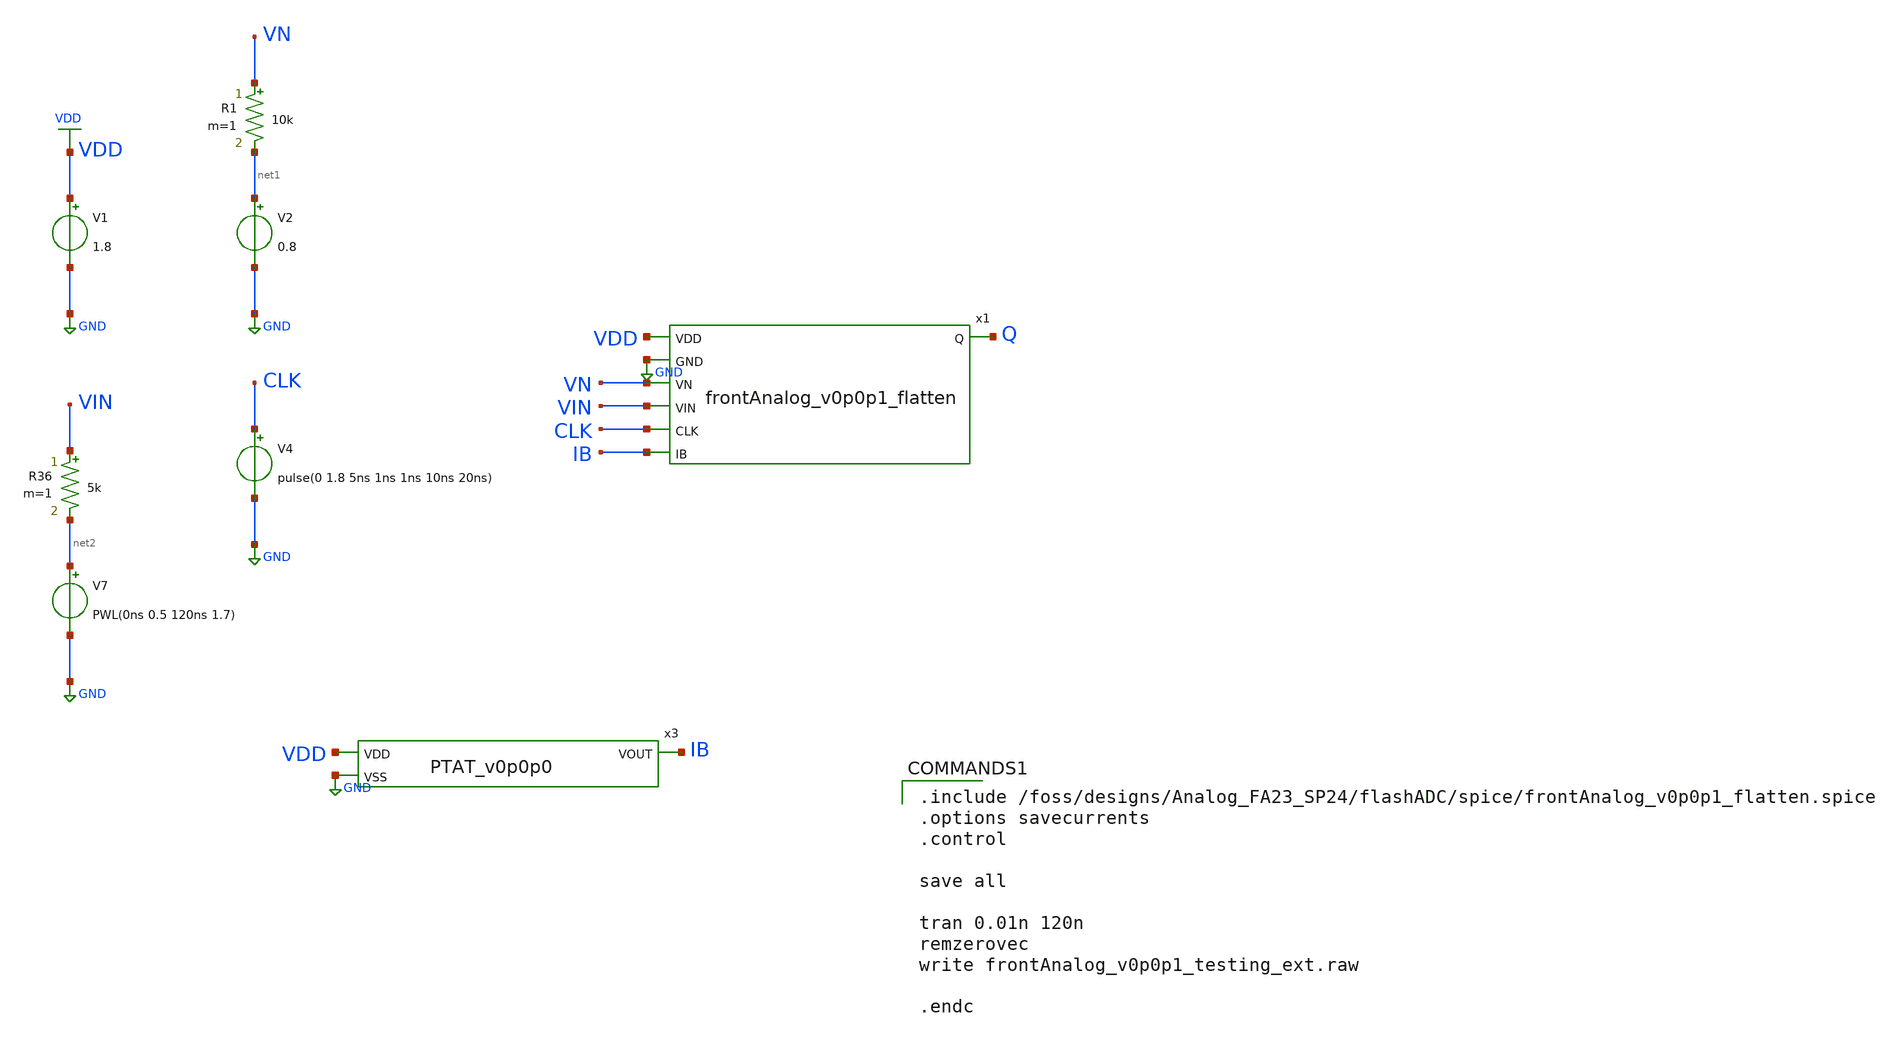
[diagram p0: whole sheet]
** sch_path: flashADC/xschem/frontAnalog_v0p0p1_testing_ext.sch
.lib $::SKYWATER_MODELS/sky130.lib.spice tt
.include $::SKYWATER_STDCELLS/sky130_fd_sc_hd.spice

**.subckt frontAnalog_v0p0p1_testing_ext
V1 VDD GND 1.8
V2 net1 GND 0.8
V4 CLK GND pulse(0 1.8 5ns 1ns 1ns 10ns 20ns)
R1 VN net1 10k m=1
V7 net2 GND PWL(0ns 0.5 120ns 1.7)
R36 VIN net2 5k m=1
x3 VDD IB GND PTAT_v0p0p0
x1 VDD GND VN VIN CLK Q IB frontAnalog_v0p0p1_flatten
**** begin user architecture code

.include /foss/designs/Analog_FA23_SP24/flashADC/spice/frontAnalog_v0p0p1_flatten.spice
.options savecurrents
.control

save all

tran 0.01n 120n
remzerovec
write frontAnalog_v0p0p1_testing_ext.raw

.endc


**** end user architecture code
**.ends
.GLOBAL GND
.GLOBAL VDD
.end
